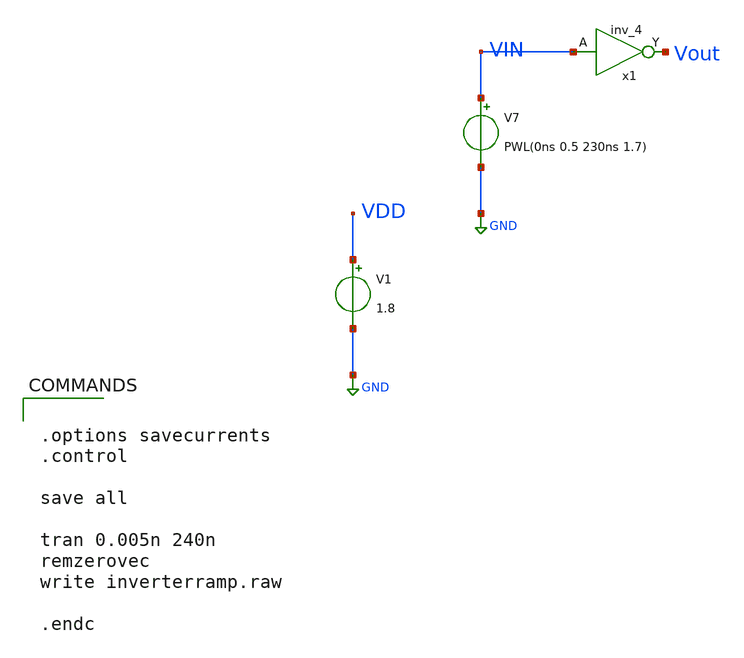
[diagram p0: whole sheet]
** sch_path: testbench/inverterramp.sch
.lib $::SKYWATER_MODELS/sky130.lib.spice fs
.include $::SKYWATER_STDCELLS/sky130_fd_sc_hd.spice

**.subckt inverterramp
x1 VIN GND GND VDD VDD Vout sky130_fd_sc_hd__inv_4
V7 VIN GND PWL(0ns 0.5 230ns 1.7)
V1 VDD GND 1.8
**** begin user architecture code


.options savecurrents
.control

save all

tran 0.005n 240n
remzerovec
write inverterramp.raw

.endc


**** end user architecture code
**.ends
.GLOBAL GND
.end
